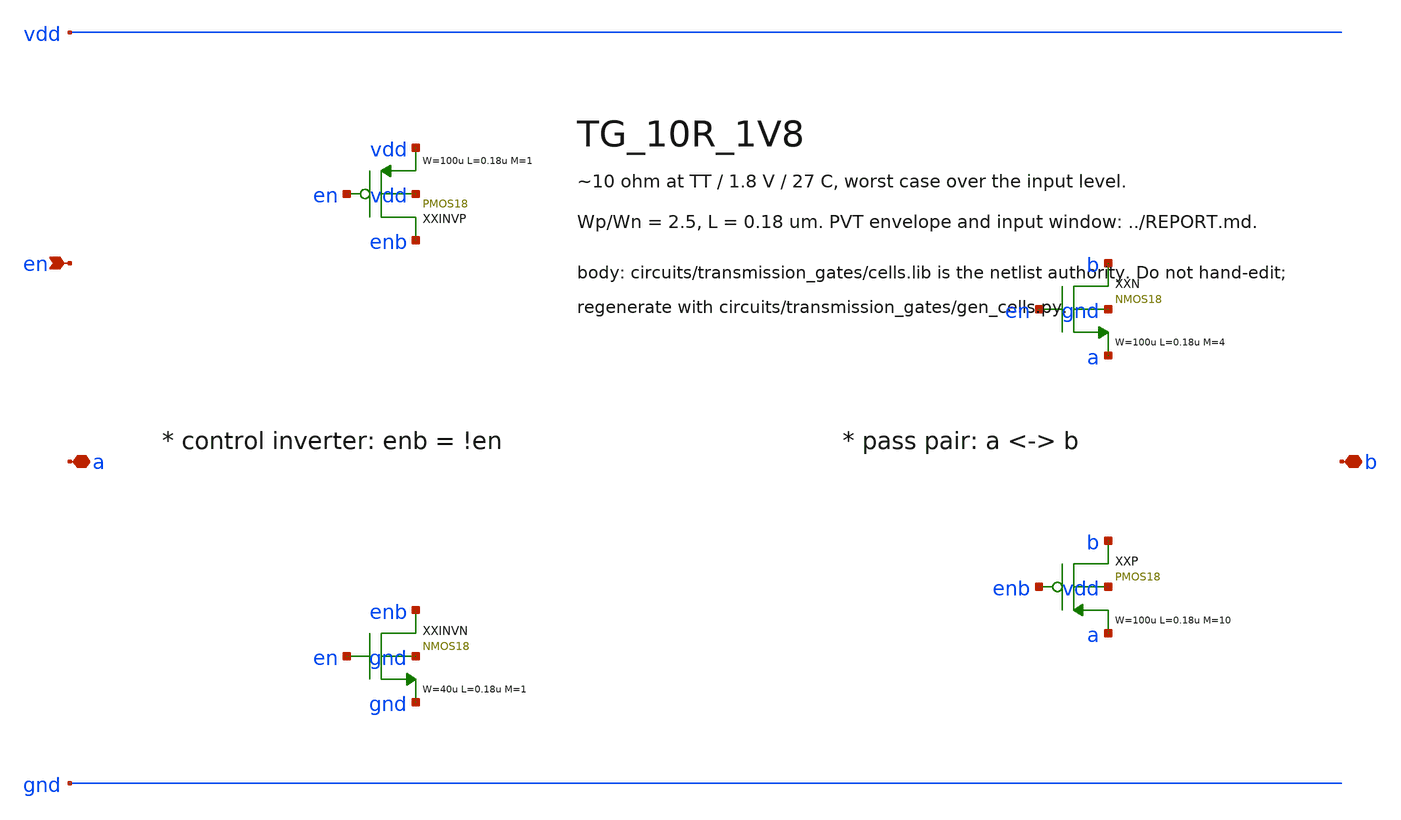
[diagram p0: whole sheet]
** sch_path: xschem/transmission_gates/TG_10R_1V8.sch
**.subckt TG_10R_1V8 a b en
*.iopin a
*.iopin b
*.ipin en
XXINVP enb en vdd vdd PMOS18 W=100u L=0.18u M=1 MM_SIGMA=0
XXINVN enb en gnd gnd NMOS18 W=40u L=0.18u M=1 MM_SIGMA=0
XXN b en a gnd NMOS18 W=100u L=0.18u M=4 MM_SIGMA=0
XXP b enb a vdd PMOS18 W=100u L=0.18u M=10 MM_SIGMA=0
**.ends
.end
